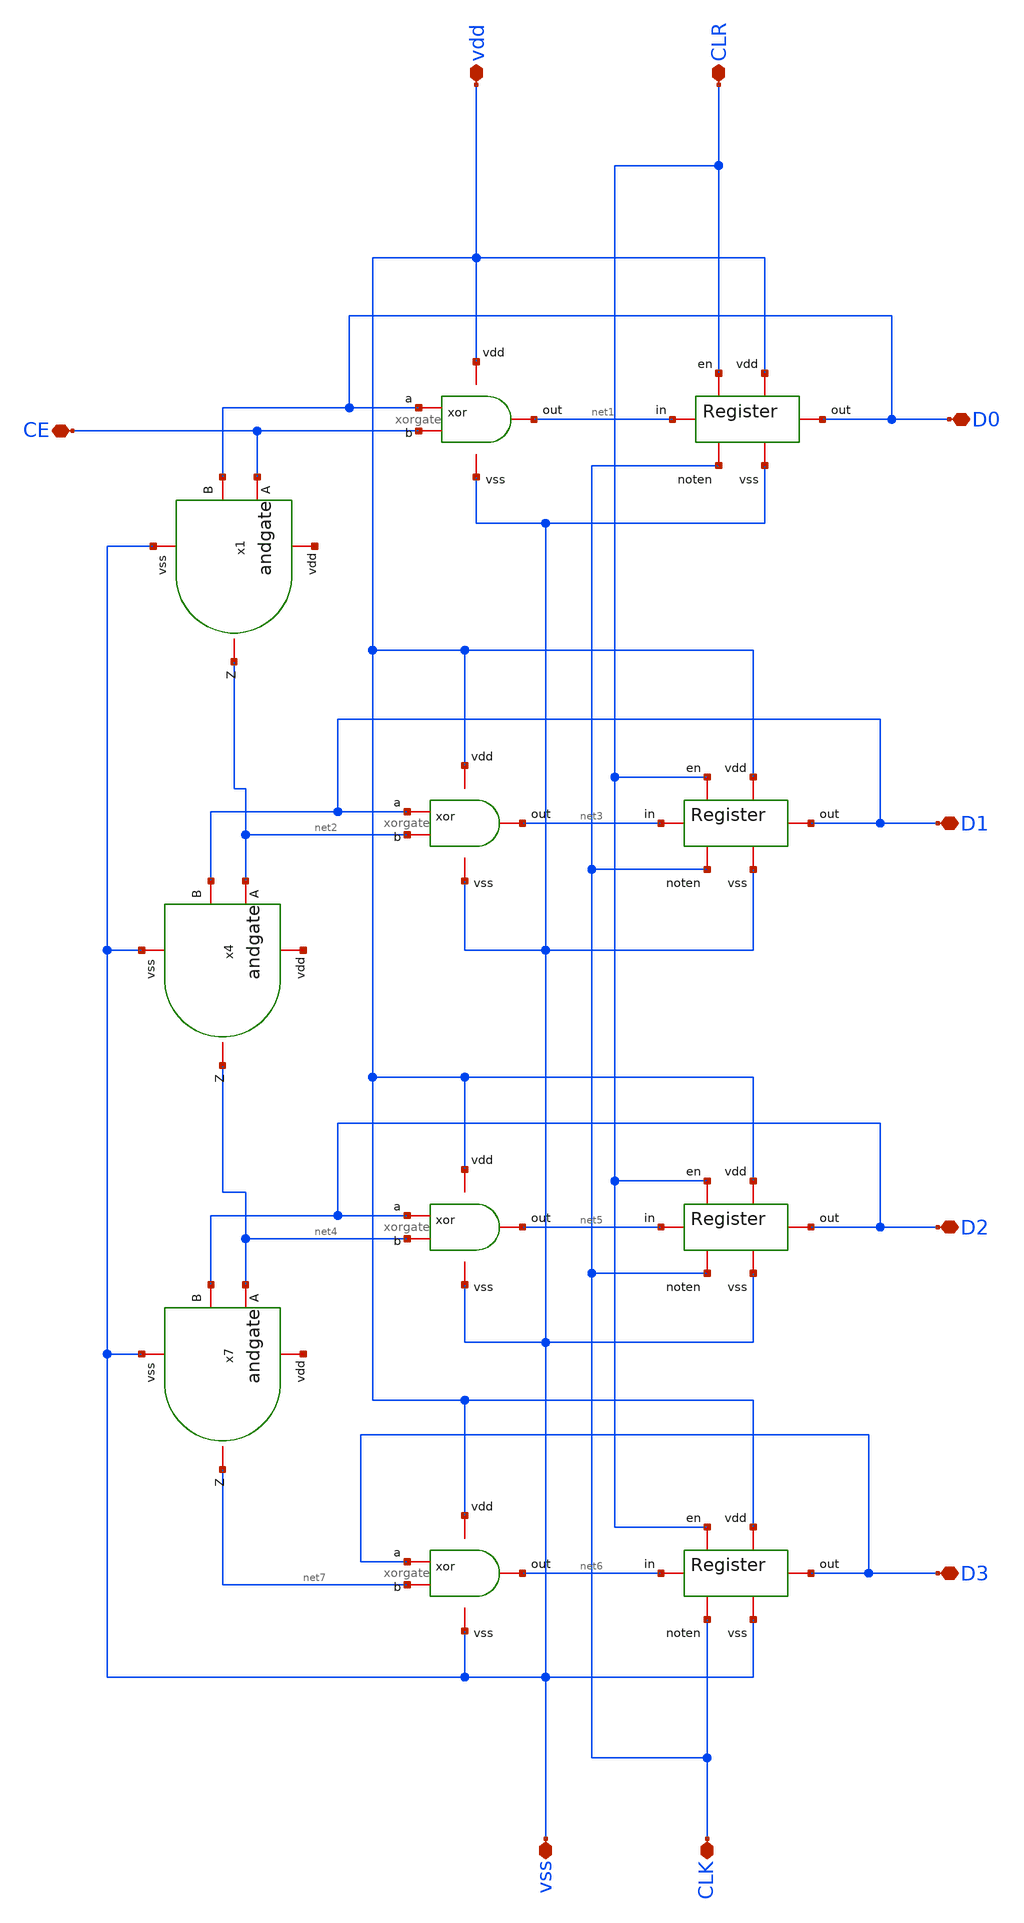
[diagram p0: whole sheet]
** sch_path: design/blocks/count4bits/schematic/count4bits.sch
**.subckt count4bits CE CLK CLR vdd vss D0 D1 D2 D3
*.iopin CE
*.iopin CLK
*.iopin CLR
*.iopin vdd
*.iopin vss
*.iopin D0
*.iopin D1
*.iopin D2
*.iopin D3
x1 net8 CE D0 net2 vss andgate
x2 D0 vdd CE vss net1 xorgate
x3 CLR CLK vss vdd D0 net1 register
x4 net9 net2 D1 net4 vss andgate
x5 D1 vdd net2 vss net3 xorgate
x6 CLR CLK vss vdd D1 net3 register
x7 net10 net4 D2 net7 vss andgate
x8 D2 vdd net4 vss net5 xorgate
x9 CLR CLK vss vdd D2 net5 register
x10 CLR CLK vss vdd D3 net6 register
x11 D3 vdd net7 vss net6 xorgate
**.ends

* expanding   symbol:  blocks/andgate/schematic/andgate.sym # of pins=5
** sym_path: design/blocks/andgate/schematic/andgate.sym
** sch_path: design/blocks/andgate/schematic/andgate.sch
.subckt andgate vdd A B Z vss
*.iopin A
*.iopin vdd
*.iopin vss
*.iopin B
*.iopin Z
XM1 net1 A vdd vdd sg13_lv_pmos w=1.0u l=0.72u ng=1 m=1 rfmode=1 mm_ok=1
XM2 vdd B net1 vdd sg13_lv_pmos w=1.0u l=0.72u ng=1 m=1 rfmode=1 mm_ok=1
XM3 net1 A net2 vss sg13_lv_nmos w=1.0u l=0.72u ng=1 m=1 rfmode=1 mm_ok=1
XM4 net2 B vss vss sg13_lv_nmos w=1.0u l=0.72u ng=1 m=1 rfmode=1 mm_ok=1
XM5 Z net1 vdd vdd sg13_lv_pmos w=1.0u l=0.72u ng=1 m=1 rfmode=1 mm_ok=1
XM6 Z net1 vss vss sg13_lv_nmos w=1.0u l=0.72u ng=1 m=1 rfmode=1 mm_ok=1
.ends


* expanding   symbol:  blocks/xorgate/schematic/xorgate.sym # of pins=5
** sym_path: design/blocks/xorgate/schematic/xorgate.sym
** sch_path: design/blocks/xorgate/schematic/xorgate.sch
.subckt xorgate a vdd b vss out
*.iopin a
*.iopin b
*.iopin vdd
*.iopin vss
*.iopin out
XM3 out a net1 vdd sg13_lv_pmos w=1.5u l=0.15u ng=1 m=1 mm_ok=1
XM1 out b net1 vdd sg13_lv_pmos w=1.5u l=0.15u ng=1 m=1 mm_ok=1
XM4 out na net2 vss sg13_lv_nmos w=1.5u l=0.15u ng=1 m=1 mm_ok=1
x1 vdd nb b vss inverter
x2 vdd na a vss inverter
XM2 net1 nb vdd vdd sg13_lv_pmos w=1.5u l=0.15u ng=1 m=1 mm_ok=1
XM5 net1 na vdd vdd sg13_lv_pmos w=1.5u l=0.15u ng=1 m=1 mm_ok=1
XM7 out a net3 vss sg13_lv_nmos w=1.5u l=0.15u ng=1 m=1 mm_ok=1
XM8 net2 nb vss vss sg13_lv_nmos w=1.5u l=0.15u ng=1 m=1 mm_ok=1
XM9 net3 b vss vss sg13_lv_nmos w=1.5u l=0.15u ng=1 m=1 mm_ok=1
.ends


* expanding   symbol:  blocks/register/schematic/register.sym # of pins=6
** sym_path: design/blocks/register/schematic/register.sym
** sch_path: design/blocks/register/schematic/register.sch
.subckt register en noten vss vdd out in
*.iopin in
*.iopin vdd
*.iopin vss
*.iopin out
*.iopin en
*.iopin noten
x1 vdd net1 in vss inverter
x3 vdd net3 net2 vss inverter
x4 vdd net4 net3 vss inverter
x5 net1 vdd noten net2 vss en transmissiongate
x6 net4 vdd noten net2 vss en transmissiongate
x7 vdd net5 net3 vss inverter
x9 vdd out net6 vss inverter
x10 vdd net7 out vss inverter
x11 net5 vdd en net6 vss noten transmissiongate
x12 net7 vdd en net6 vss noten transmissiongate
.ends


* expanding   symbol:  blocks/inverter/schematic/inverter.sym # of pins=4
** sym_path: design/blocks/inverter/schematic/inverter.sym
** sch_path: design/blocks/inverter/schematic/inverter.sch
.subckt inverter vdd out in vss
*.iopin vdd
*.iopin out
*.iopin vss
*.iopin in
XM1 out in vss vss sg13_lv_nmos w=0.75u l=0.15u ng=1 m=1 mm_ok=1
XM2 out in vdd vdd sg13_lv_pmos w=1.5u l=0.15u ng=1 m=1 mm_ok=1
.ends


* expanding   symbol:  blocks/transmissiongate/schematic/transmissiongate.sym # of pins=6
** sym_path: design/blocks/transmissiongate/schematic/transmissiongate.sym
** sch_path: design/blocks/transmissiongate/schematic/transmissiongate.sch
.subckt transmissiongate in vdd noten out vss en
*.iopin noten
*.iopin en
*.iopin in
*.iopin out
*.iopin vdd
*.iopin vss
XM1 out noten in vdd sg13_lv_pmos w=1.5u l=0.15u ng=1 m=1 mm_ok=1
XM2 out en in vss sg13_lv_nmos w=0.75u l=0.15u ng=1 m=1 mm_ok=1
.ends

.end
